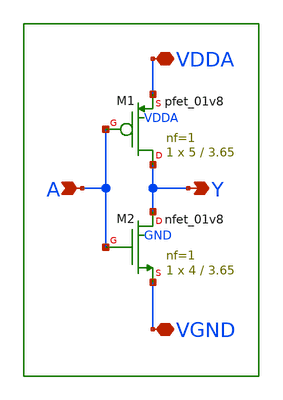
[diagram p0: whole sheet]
** sch_path: xschem/lib/old_aux_inv.sch
**.subckt old_aux_inv VDDA VGND A Y
*.iopin VDDA
*.iopin VGND
*.ipin A
*.opin Y
XM1 Y A VDDA VDDA sky130_fd_pr__pfet_01v8 L=3.65 W=5 nf=1 ad='int((1 + 1)/2) * 5 / 1 * 0.29' as='int((1 + 2)/2) * 5 / 1 * 0.29'
+ pd='2*int((1 + 1)/2) * (5 / 1 + 0.29)' ps='2*int((1 + 2)/2) * (5 / 1 + 0.29)' nrd='0.29 / 5 ' nrs='0.29 / 5 '
+ sa=0 sb=0 sd=0 mult=1 m=1
XM2 Y A VGND GND sky130_fd_pr__nfet_01v8 L=3.65 W=4 nf=1 ad='int((nf+1)/2) * W/nf * 0.29' as='int((nf+2)/2) * W/nf * 0.29'
+ pd='2*int((nf+1)/2) * (W/nf + 0.29)' ps='2*int((nf+2)/2) * (W/nf + 0.29)' nrd='0.29 / W' nrs='0.29 / W'
+ sa=0 sb=0 sd=0 mult=1 m=1
**.ends
.end
